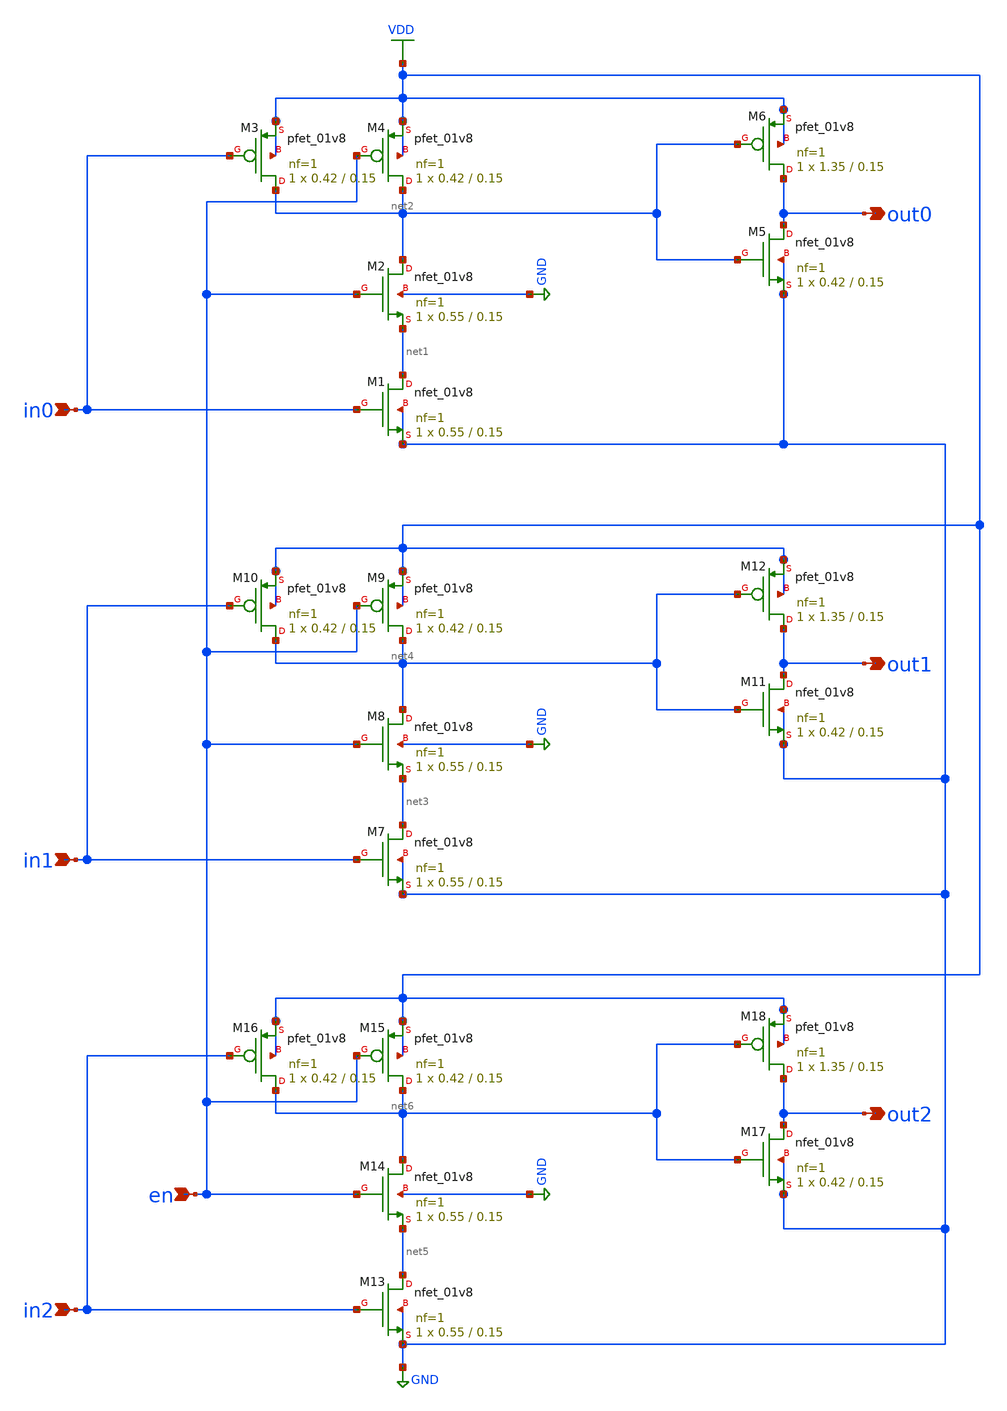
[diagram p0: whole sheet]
** sch_path: xschem/wordline_driver.sch
**.subckt wordline_driver in0 in1 in2 en out1 out0 out2
*.ipin in0
*.ipin in1
*.ipin in2
*.ipin en
*.opin out1
*.opin out0
*.opin out2
XM1 net1 in0 GND GND sky130_fd_pr__nfet_01v8 L=0.15 W=0.55 nf=1 ad='int((nf+1)/2) * W/nf * 0.29' as='int((nf+2)/2) * W/nf * 0.29'
+ pd='2*int((nf+1)/2) * (W/nf + 0.29)' ps='2*int((nf+2)/2) * (W/nf + 0.29)' nrd='0.29 / W' nrs='0.29 / W'
+ sa=0 sb=0 sd=0 mult=1 m=1
XM2 net2 en net1 GND sky130_fd_pr__nfet_01v8 L=0.15 W=0.55 nf=1 ad='int((nf+1)/2) * W/nf * 0.29' as='int((nf+2)/2) * W/nf * 0.29'
+ pd='2*int((nf+1)/2) * (W/nf + 0.29)' ps='2*int((nf+2)/2) * (W/nf + 0.29)' nrd='0.29 / W' nrs='0.29 / W'
+ sa=0 sb=0 sd=0 mult=1 m=1
XM4 net2 en VDD VDD sky130_fd_pr__pfet_01v8 L=0.15 W=0.42 nf=1 ad='int((nf+1)/2) * W/nf * 0.29' as='int((nf+2)/2) * W/nf * 0.29'
+ pd='2*int((nf+1)/2) * (W/nf + 0.29)' ps='2*int((nf+2)/2) * (W/nf + 0.29)' nrd='0.29 / W' nrs='0.29 / W'
+ sa=0 sb=0 sd=0 mult=1 m=1
XM3 net2 in0 VDD VDD sky130_fd_pr__pfet_01v8 L=0.15 W=0.42 nf=1 ad='int((nf+1)/2) * W/nf * 0.29' as='int((nf+2)/2) * W/nf * 0.29'
+ pd='2*int((nf+1)/2) * (W/nf + 0.29)' ps='2*int((nf+2)/2) * (W/nf + 0.29)' nrd='0.29 / W' nrs='0.29 / W'
+ sa=0 sb=0 sd=0 mult=1 m=1
XM5 out0 net2 GND GND sky130_fd_pr__nfet_01v8 L=0.15 W=0.42 nf=1 ad='int((nf+1)/2) * W/nf * 0.29' as='int((nf+2)/2) * W/nf * 0.29'
+ pd='2*int((nf+1)/2) * (W/nf + 0.29)' ps='2*int((nf+2)/2) * (W/nf + 0.29)' nrd='0.29 / W' nrs='0.29 / W'
+ sa=0 sb=0 sd=0 mult=1 m=1
XM6 out0 net2 VDD VDD sky130_fd_pr__pfet_01v8 L=0.15 W=1.35 nf=1 ad='int((nf+1)/2) * W/nf * 0.29' as='int((nf+2)/2) * W/nf * 0.29'
+ pd='2*int((nf+1)/2) * (W/nf + 0.29)' ps='2*int((nf+2)/2) * (W/nf + 0.29)' nrd='0.29 / W' nrs='0.29 / W'
+ sa=0 sb=0 sd=0 mult=1 m=1
XM7 net3 in1 GND GND sky130_fd_pr__nfet_01v8 L=0.15 W=0.55 nf=1 ad='int((nf+1)/2) * W/nf * 0.29' as='int((nf+2)/2) * W/nf * 0.29'
+ pd='2*int((nf+1)/2) * (W/nf + 0.29)' ps='2*int((nf+2)/2) * (W/nf + 0.29)' nrd='0.29 / W' nrs='0.29 / W'
+ sa=0 sb=0 sd=0 mult=1 m=1
XM8 net4 en net3 GND sky130_fd_pr__nfet_01v8 L=0.15 W=0.55 nf=1 ad='int((nf+1)/2) * W/nf * 0.29' as='int((nf+2)/2) * W/nf * 0.29'
+ pd='2*int((nf+1)/2) * (W/nf + 0.29)' ps='2*int((nf+2)/2) * (W/nf + 0.29)' nrd='0.29 / W' nrs='0.29 / W'
+ sa=0 sb=0 sd=0 mult=1 m=1
XM9 net4 en VDD VDD sky130_fd_pr__pfet_01v8 L=0.15 W=0.42 nf=1 ad='int((nf+1)/2) * W/nf * 0.29' as='int((nf+2)/2) * W/nf * 0.29'
+ pd='2*int((nf+1)/2) * (W/nf + 0.29)' ps='2*int((nf+2)/2) * (W/nf + 0.29)' nrd='0.29 / W' nrs='0.29 / W'
+ sa=0 sb=0 sd=0 mult=1 m=1
XM10 net4 in1 VDD VDD sky130_fd_pr__pfet_01v8 L=0.15 W=0.42 nf=1 ad='int((nf+1)/2) * W/nf * 0.29' as='int((nf+2)/2) * W/nf * 0.29'
+ pd='2*int((nf+1)/2) * (W/nf + 0.29)' ps='2*int((nf+2)/2) * (W/nf + 0.29)' nrd='0.29 / W' nrs='0.29 / W'
+ sa=0 sb=0 sd=0 mult=1 m=1
XM11 out1 net4 GND GND sky130_fd_pr__nfet_01v8 L=0.15 W=0.42 nf=1 ad='int((nf+1)/2) * W/nf * 0.29' as='int((nf+2)/2) * W/nf * 0.29'
+ pd='2*int((nf+1)/2) * (W/nf + 0.29)' ps='2*int((nf+2)/2) * (W/nf + 0.29)' nrd='0.29 / W' nrs='0.29 / W'
+ sa=0 sb=0 sd=0 mult=1 m=1
XM12 out1 net4 VDD VDD sky130_fd_pr__pfet_01v8 L=0.15 W=1.35 nf=1 ad='int((nf+1)/2) * W/nf * 0.29' as='int((nf+2)/2) * W/nf * 0.29'
+ pd='2*int((nf+1)/2) * (W/nf + 0.29)' ps='2*int((nf+2)/2) * (W/nf + 0.29)' nrd='0.29 / W' nrs='0.29 / W'
+ sa=0 sb=0 sd=0 mult=1 m=1
XM13 net5 in2 GND GND sky130_fd_pr__nfet_01v8 L=0.15 W=0.55 nf=1 ad='int((nf+1)/2) * W/nf * 0.29' as='int((nf+2)/2) * W/nf * 0.29'
+ pd='2*int((nf+1)/2) * (W/nf + 0.29)' ps='2*int((nf+2)/2) * (W/nf + 0.29)' nrd='0.29 / W' nrs='0.29 / W'
+ sa=0 sb=0 sd=0 mult=1 m=1
XM14 net6 en net5 GND sky130_fd_pr__nfet_01v8 L=0.15 W=0.55 nf=1 ad='int((nf+1)/2) * W/nf * 0.29' as='int((nf+2)/2) * W/nf * 0.29'
+ pd='2*int((nf+1)/2) * (W/nf + 0.29)' ps='2*int((nf+2)/2) * (W/nf + 0.29)' nrd='0.29 / W' nrs='0.29 / W'
+ sa=0 sb=0 sd=0 mult=1 m=1
XM15 net6 en VDD VDD sky130_fd_pr__pfet_01v8 L=0.15 W=0.42 nf=1 ad='int((nf+1)/2) * W/nf * 0.29' as='int((nf+2)/2) * W/nf * 0.29'
+ pd='2*int((nf+1)/2) * (W/nf + 0.29)' ps='2*int((nf+2)/2) * (W/nf + 0.29)' nrd='0.29 / W' nrs='0.29 / W'
+ sa=0 sb=0 sd=0 mult=1 m=1
XM16 net6 in2 VDD VDD sky130_fd_pr__pfet_01v8 L=0.15 W=0.42 nf=1 ad='int((nf+1)/2) * W/nf * 0.29' as='int((nf+2)/2) * W/nf * 0.29'
+ pd='2*int((nf+1)/2) * (W/nf + 0.29)' ps='2*int((nf+2)/2) * (W/nf + 0.29)' nrd='0.29 / W' nrs='0.29 / W'
+ sa=0 sb=0 sd=0 mult=1 m=1
XM17 out2 net6 GND GND sky130_fd_pr__nfet_01v8 L=0.15 W=0.42 nf=1 ad='int((nf+1)/2) * W/nf * 0.29' as='int((nf+2)/2) * W/nf * 0.29'
+ pd='2*int((nf+1)/2) * (W/nf + 0.29)' ps='2*int((nf+2)/2) * (W/nf + 0.29)' nrd='0.29 / W' nrs='0.29 / W'
+ sa=0 sb=0 sd=0 mult=1 m=1
XM18 out2 net6 VDD VDD sky130_fd_pr__pfet_01v8 L=0.15 W=1.35 nf=1 ad='int((nf+1)/2) * W/nf * 0.29' as='int((nf+2)/2) * W/nf * 0.29'
+ pd='2*int((nf+1)/2) * (W/nf + 0.29)' ps='2*int((nf+2)/2) * (W/nf + 0.29)' nrd='0.29 / W' nrs='0.29 / W'
+ sa=0 sb=0 sd=0 mult=1 m=1
**.ends
.GLOBAL GND
.GLOBAL VDD
.end
